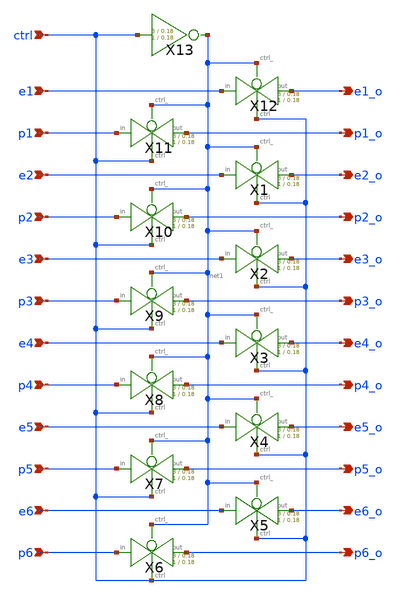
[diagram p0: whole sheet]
** sch_path: xschem/readout/switch_ro.sch
**.subckt switch_ro ctrl e1 e2 e3 e4 e5 e6 p1 p2 p3 p4 p5 p6 e1_o e2_o e3_o e4_o e5_o e6_o p1_o p2_o
*+ p3_o p4_o p5_o p6_o
*.ipin ctrl
*.ipin e1
*.ipin e2
*.ipin e3
*.ipin e4
*.ipin e5
*.ipin e6
*.ipin p1
*.ipin p2
*.ipin p3
*.ipin p4
*.ipin p5
*.ipin p6
*.opin e1_o
*.opin e2_o
*.opin e3_o
*.opin e4_o
*.opin e5_o
*.opin e6_o
*.opin p1_o
*.opin p2_o
*.opin p3_o
*.opin p4_o
*.opin p5_o
*.opin p6_o
X12 e1 e1_o net1 ctrl transmission_gate Wpmos=3 Lpmos=0.18 Wnmos=1 Lnmos=0.18
X13 ctrl net1 inv Wpmos=3 Lpmos=0.18 Wnmos=1 Lnmos=0.18
X1 e2 e2_o net1 ctrl transmission_gate Wpmos=3 Lpmos=0.18 Wnmos=1 Lnmos=0.18
X2 e3 e3_o net1 ctrl transmission_gate Wpmos=3 Lpmos=0.18 Wnmos=1 Lnmos=0.18
X3 e4 e4_o net1 ctrl transmission_gate Wpmos=3 Lpmos=0.18 Wnmos=1 Lnmos=0.18
X4 e5 e5_o net1 ctrl transmission_gate Wpmos=3 Lpmos=0.18 Wnmos=1 Lnmos=0.18
X5 e6 e6_o net1 ctrl transmission_gate Wpmos=3 Lpmos=0.18 Wnmos=1 Lnmos=0.18
X6 p6 p6_o net1 ctrl transmission_gate Wpmos=3 Lpmos=0.18 Wnmos=1 Lnmos=0.18
X7 p5 p5_o net1 ctrl transmission_gate Wpmos=3 Lpmos=0.18 Wnmos=1 Lnmos=0.18
X8 p4 p4_o net1 ctrl transmission_gate Wpmos=3 Lpmos=0.18 Wnmos=1 Lnmos=0.18
X9 p3 p3_o net1 ctrl transmission_gate Wpmos=3 Lpmos=0.18 Wnmos=1 Lnmos=0.18
X10 p2 p2_o net1 ctrl transmission_gate Wpmos=3 Lpmos=0.18 Wnmos=1 Lnmos=0.18
X11 p1 p1_o net1 ctrl transmission_gate Wpmos=3 Lpmos=0.18 Wnmos=1 Lnmos=0.18
**.ends

* expanding   symbol:  transmission_gate/transmission_gate.sym # of pins=4
** sym_path: xschem/transmission_gate/transmission_gate.sym
** sch_path: xschem/transmission_gate/transmission_gate.sch
.subckt transmission_gate in out ctrl_ ctrl  Wpmos=0.42 Lpmos=0.18 Wnmos=0.42 Lnmos=0.18
*.iopin in
*.iopin out
*.ipin ctrl_
*.ipin ctrl
XM1 out ctrl in GND sky130_fd_pr__nfet_01v8 L=Lnmos W=Wnmos nf=1 ad='int((nf+1)/2) * W/nf * 0.29' as='int((nf+2)/2) * W/nf * 0.29'
+ pd='2*int((nf+1)/2) * (W/nf + 0.29)' ps='2*int((nf+2)/2) * (W/nf + 0.29)' nrd='0.29 / W' nrs='0.29 / W'
+ sa=0 sb=0 sd=0 mult=1 m=1
XM2 out ctrl_ in VDD sky130_fd_pr__pfet_01v8 L=Lpmos W=Wpmos nf=1 ad='int((nf+1)/2) * W/nf * 0.29' as='int((nf+2)/2) * W/nf * 0.29'
+ pd='2*int((nf+1)/2) * (W/nf + 0.29)' ps='2*int((nf+2)/2) * (W/nf + 0.29)' nrd='0.29 / W' nrs='0.29 / W'
+ sa=0 sb=0 sd=0 mult=1 m=1
.ends


* expanding   symbol:  inv/inv.sym # of pins=2
** sym_path: xschem/inv/inv.sym
** sch_path: xschem/inv/inv.sch
.subckt inv in out  Wpmos=3 Lpmos=0.18 Wnmos=1 Lnmos=0.18
*.ipin in
*.iopin out
XM1 out in GND GND sky130_fd_pr__nfet_01v8 L=Lnmos W=Wnmos nf=1 ad='int((nf+1)/2) * W/nf * 0.29' as='int((nf+2)/2) * W/nf * 0.29'
+ pd='2*int((nf+1)/2) * (W/nf + 0.29)' ps='2*int((nf+2)/2) * (W/nf + 0.29)' nrd='0.29 / W' nrs='0.29 / W'
+ sa=0 sb=0 sd=0 mult=1 m=1
XM2 out in VDD VDD sky130_fd_pr__pfet_01v8 L=Lpmos W=Wpmos nf=1 ad='int((nf+1)/2) * W/nf * 0.29' as='int((nf+2)/2) * W/nf * 0.29'
+ pd='2*int((nf+1)/2) * (W/nf + 0.29)' ps='2*int((nf+2)/2) * (W/nf + 0.29)' nrd='0.29 / W' nrs='0.29 / W'
+ sa=0 sb=0 sd=0 mult=1 m=1
.ends

.GLOBAL GND
.GLOBAL VDD
.end
